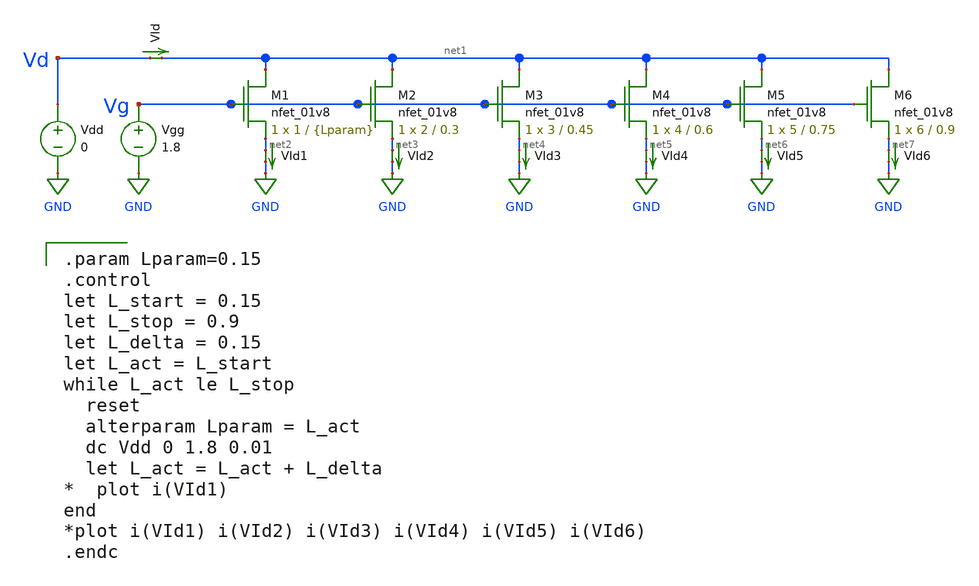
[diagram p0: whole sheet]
** sch_path: mini4/schem/earlytest.sch
**.subckt earlytest
Vdd Vd GND 0
Vgg Vg GND 1.8
VId Vd net1 0
.save i(vid)
XM1 net1 Vg net2 GND sky130_fd_pr__nfet_01v8 L={Lparam} W=1 nf=1 ad='int((nf+1)/2) * W/nf * 0.29' as='int((nf+2)/2) * W/nf * 0.29'
+ pd='2*int((nf+1)/2) * (W/nf + 0.29)' ps='2*int((nf+2)/2) * (W/nf + 0.29)' nrd='0.29 / W' nrs='0.29 / W'
+ sa=0 sb=0 sd=0 mult=1 m=1
XM2 net1 Vg net3 GND sky130_fd_pr__nfet_01v8 L=0.3 W=2 nf=1 ad='int((nf+1)/2) * W/nf * 0.29' as='int((nf+2)/2) * W/nf * 0.29'
+ pd='2*int((nf+1)/2) * (W/nf + 0.29)' ps='2*int((nf+2)/2) * (W/nf + 0.29)' nrd='0.29 / W' nrs='0.29 / W'
+ sa=0 sb=0 sd=0 mult=1 m=1
XM3 net1 Vg net4 GND sky130_fd_pr__nfet_01v8 L=0.45 W=3 nf=1 ad='int((nf+1)/2) * W/nf * 0.29' as='int((nf+2)/2) * W/nf * 0.29'
+ pd='2*int((nf+1)/2) * (W/nf + 0.29)' ps='2*int((nf+2)/2) * (W/nf + 0.29)' nrd='0.29 / W' nrs='0.29 / W'
+ sa=0 sb=0 sd=0 mult=1 m=1
XM4 net1 Vg net5 GND sky130_fd_pr__nfet_01v8 L=0.6 W=4 nf=1 ad='int((nf+1)/2) * W/nf * 0.29' as='int((nf+2)/2) * W/nf * 0.29'
+ pd='2*int((nf+1)/2) * (W/nf + 0.29)' ps='2*int((nf+2)/2) * (W/nf + 0.29)' nrd='0.29 / W' nrs='0.29 / W'
+ sa=0 sb=0 sd=0 mult=1 m=1
VId1 net2 GND 0
.save i(vid1)
VId2 net3 GND 0
.save i(vid2)
VId3 net4 GND 0
.save i(vid3)
VId4 net5 GND 0
.save i(vid4)
XM5 net1 Vg net6 GND sky130_fd_pr__nfet_01v8 L=0.75 W=5 nf=1 ad='int((nf+1)/2) * W/nf * 0.29' as='int((nf+2)/2) * W/nf * 0.29'
+ pd='2*int((nf+1)/2) * (W/nf + 0.29)' ps='2*int((nf+2)/2) * (W/nf + 0.29)' nrd='0.29 / W' nrs='0.29 / W'
+ sa=0 sb=0 sd=0 mult=1 m=1
XM6 net1 Vg net7 GND sky130_fd_pr__nfet_01v8 L=0.9 W=6 nf=1 ad='int((nf+1)/2) * W/nf * 0.29' as='int((nf+2)/2) * W/nf * 0.29'
+ pd='2*int((nf+1)/2) * (W/nf + 0.29)' ps='2*int((nf+2)/2) * (W/nf + 0.29)' nrd='0.29 / W' nrs='0.29 / W'
+ sa=0 sb=0 sd=0 mult=1 m=1
VId5 net6 GND 0
.save i(vid5)
VId6 net7 GND 0
.save i(vid6)
**** begin user architecture code

.option wnflag=1
.param MC_SWITCH=0.0
.lib ~/skywater/skywater-pdk/libraries/sky130_fd_pr_ngspice/latest/models/sky130.lib.spice tt


.param Lparam=0.15
.control
let L_start = 0.15
let L_stop = 0.9
let L_delta = 0.15
let L_act = L_start
while L_act le L_stop
  reset
  alterparam Lparam = L_act
  dc Vdd 0 1.8 0.01
  let L_act = L_act + L_delta
*  plot i(VId1)
end
*plot i(VId1) i(VId2) i(VId3) i(VId4) i(VId5) i(VId6)
.endc

**** end user architecture code
**.ends
.GLOBAL GND
.end
